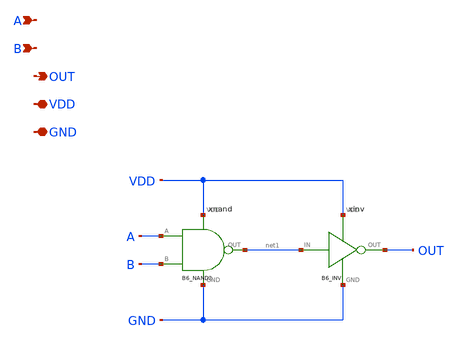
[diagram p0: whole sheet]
** sch_path: blocks/06_Clock_gen/xschem/B6_AND2.sch
**.subckt B6_AND2 A B OUT VDD GND
*.ipin A
*.ipin B
*.opin OUT
*.iopin VDD
*.iopin GND
xnand A B net1 VDD GND B6_NAND2
xinv net1 OUT VDD GND B6_INV
**.ends

* expanding   symbol:  blocks/06_Clock_gen/xschem/B6_NAND2.sym # of pins=5
** sym_path: blocks/06_Clock_gen/xschem/B6_NAND2.sym
** sch_path: blocks/06_Clock_gen/xschem/B6_NAND2.sch
.subckt B6_NAND2 A B OUT VDD GND
*.ipin A
*.ipin B
*.opin OUT
*.iopin VDD
*.iopin GND
XMPA VDD A OUT VDD sky130_fd_pr__pfet_01v8 L=0.15 W=2 nf=1 ad='int((1 + 1)/2) * 2 / 1 * 0.29' as='int((1 + 2)/2) * 2 / 1 * 0.29'
+ pd='2*int((1 + 1)/2) * (2 / 1 + 0.29)' ps='2*int((1 + 2)/2) * (2 / 1 + 0.29)' nrd='0.29 / 2 ' nrs='0.29 / 2 '
+ sa=0 sb=0 sd=0 mult=1 m=1
XMPB VDD B OUT VDD sky130_fd_pr__pfet_01v8 L=0.15 W=2 nf=1 ad='int((1 + 1)/2) * 2 / 1 * 0.29' as='int((1 + 2)/2) * 2 / 1 * 0.29'
+ pd='2*int((1 + 1)/2) * (2 / 1 + 0.29)' ps='2*int((1 + 2)/2) * (2 / 1 + 0.29)' nrd='0.29 / 2 ' nrs='0.29 / 2 '
+ sa=0 sb=0 sd=0 mult=1 m=1
XMNA OUT A net1 GND sky130_fd_pr__nfet_01v8 L=0.15 W=2 nf=1 ad='int((1 + 1)/2) * 2 / 1 * 0.29' as='int((1 + 2)/2) * 2 / 1 * 0.29'
+ pd='2*int((1 + 1)/2) * (2 / 1 + 0.29)' ps='2*int((1 + 2)/2) * (2 / 1 + 0.29)' nrd='0.29 / 2 ' nrs='0.29 / 2 '
+ sa=0 sb=0 sd=0 mult=1 m=1
XMNB net1 B GND GND sky130_fd_pr__nfet_01v8 L=0.15 W=2 nf=1 ad='int((1 + 1)/2) * 2 / 1 * 0.29' as='int((1 + 2)/2) * 2 / 1 * 0.29'
+ pd='2*int((1 + 1)/2) * (2 / 1 + 0.29)' ps='2*int((1 + 2)/2) * (2 / 1 + 0.29)' nrd='0.29 / 2 ' nrs='0.29 / 2 '
+ sa=0 sb=0 sd=0 mult=1 m=1
.ends


* expanding   symbol:  blocks/06_Clock_gen/xschem/B6_INV.sym # of pins=4
** sym_path: blocks/06_Clock_gen/xschem/B6_INV.sym
** sch_path: blocks/06_Clock_gen/xschem/B6_INV.sch
.subckt B6_INV IN OUT VDD GND
*.ipin IN
*.opin OUT
*.iopin VDD
*.iopin GND
XMP VDD IN OUT VDD sky130_fd_pr__pfet_01v8 L=0.15 W=2 nf=1 ad='int((1 + 1)/2) * 2 / 1 * 0.29' as='int((1 + 2)/2) * 2 / 1 * 0.29'
+ pd='2*int((1 + 1)/2) * (2 / 1 + 0.29)' ps='2*int((1 + 2)/2) * (2 / 1 + 0.29)' nrd='0.29 / 2 ' nrs='0.29 / 2 '
+ sa=0 sb=0 sd=0 mult=1 m=1
XMN OUT IN GND GND sky130_fd_pr__nfet_01v8 L=0.15 W=1 nf=1 ad='int((1 + 1)/2) * 1 / 1 * 0.29' as='int((1 + 2)/2) * 1 / 1 * 0.29'
+ pd='2*int((1 + 1)/2) * (1 / 1 + 0.29)' ps='2*int((1 + 2)/2) * (1 / 1 + 0.29)' nrd='0.29 / 1 ' nrs='0.29 / 1 '
+ sa=0 sb=0 sd=0 mult=1 m=1
.ends

.end
